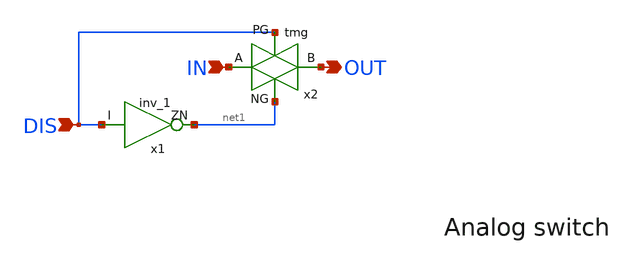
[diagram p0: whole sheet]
** sch_path: PLL/xschem/sw.sch
**.subckt sw OUT IN DIS
*.opin OUT
*.ipin IN
*.ipin DIS
x1 DIS net1 VDD VDD GND GND gf180mcu_fd_sc_mcu7t5v0__inv_1
x2 DIS OUT IN net1 tmg
**.ends

* expanding   symbol:  tmg.sym # of pins=4
** sym_path: PLL/xschem/tmg.sym
** sch_path: PLL/xschem/tmg.sch
.subckt tmg PG B A NG
*.opin B
*.ipin A
*.ipin PG
*.ipin NG
XM3 B PG A VDD pfet_06v0 L=0.50u W=2u nf=1 ad='int((nf+1)/2) * W/nf * 0.18u' as='int((nf+2)/2) * W/nf * 0.18u'
+ pd='2*int((nf+1)/2) * (W/nf + 0.18u)' ps='2*int((nf+2)/2) * (W/nf + 0.18u)' nrd='0.18u / W' nrs='0.18u / W'
+ sa=0 sb=0 sd=0 m=1
XM4 A NG B GND nfet_06v0 L=0.60u W=0.9u nf=1 ad='int((nf+1)/2) * W/nf * 0.18u' as='int((nf+2)/2) * W/nf * 0.18u'
+ pd='2*int((nf+1)/2) * (W/nf + 0.18u)' ps='2*int((nf+2)/2) * (W/nf + 0.18u)' nrd='0.18u / W' nrs='0.18u / W'
+ sa=0 sb=0 sd=0 m=1
.ends

.GLOBAL GND
.GLOBAL VDD
.end
